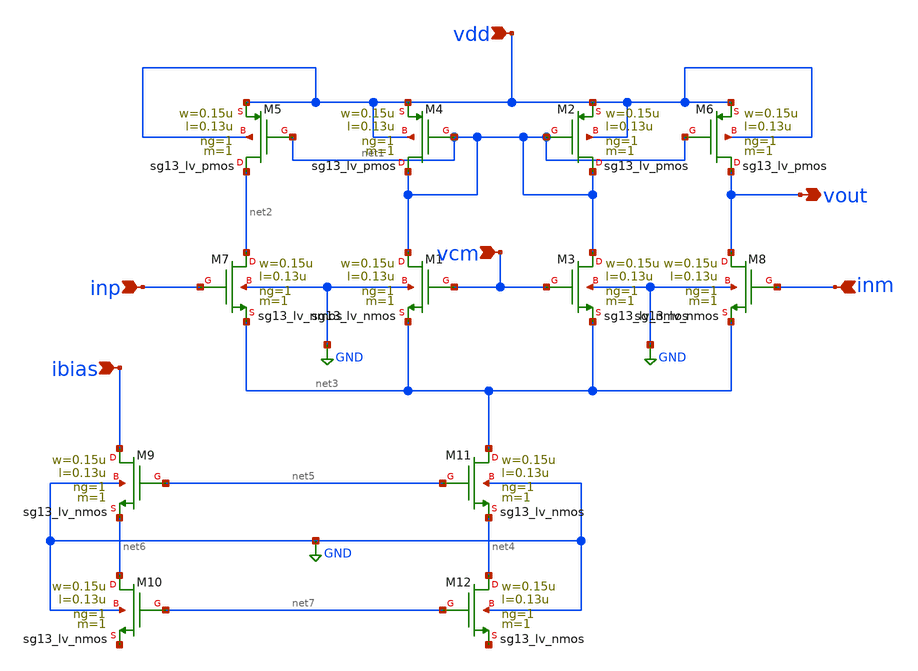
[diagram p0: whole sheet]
** sch_path: 3_Real_Cir/10_Real_Cir/untitled-2.sch
**.subckt untitled-2 inp vdd inm vout vcm ibias
*.ipin inp
*.ipin vdd
*.ipin inm
*.opin vout
*.ipin vcm
*.ipin ibias
XM1 net1 vcm net3 GND sg13_lv_nmos w=0.15u l=0.13u ng=1 m=1 mm_ok=1
XM2 net1 net1 vdd vdd sg13_lv_pmos w=0.15u l=0.13u ng=1 m=1 mm_ok=1
XM3 net1 vcm net3 GND sg13_lv_nmos w=0.15u l=0.13u ng=1 m=1 mm_ok=1
XM4 net1 net1 vdd vdd sg13_lv_pmos w=0.15u l=0.13u ng=1 m=1 mm_ok=1
XM5 net2 net1 vdd vdd sg13_lv_pmos w=0.15u l=0.13u ng=1 m=1 mm_ok=1
XM6 vout net1 vdd vdd sg13_lv_pmos w=0.15u l=0.13u ng=1 m=1 mm_ok=1
XM7 net2 inp net3 GND sg13_lv_nmos w=0.15u l=0.13u ng=1 m=1 mm_ok=1
XM8 vout inm net3 GND sg13_lv_nmos w=0.15u l=0.13u ng=1 m=1 mm_ok=1
XM9 ibias net5 net6 GND sg13_lv_nmos w=0.15u l=0.13u ng=1 m=1 mm_ok=1
XM11 net3 net5 net4 GND sg13_lv_nmos w=0.15u l=0.13u ng=1 m=1 mm_ok=1
XM10 net6 net7 net8 GND sg13_lv_nmos w=0.15u l=0.13u ng=1 m=1 mm_ok=1
XM12 net4 net7 net9 GND sg13_lv_nmos w=0.15u l=0.13u ng=1 m=1 mm_ok=1
**.ends
.GLOBAL GND
.end
